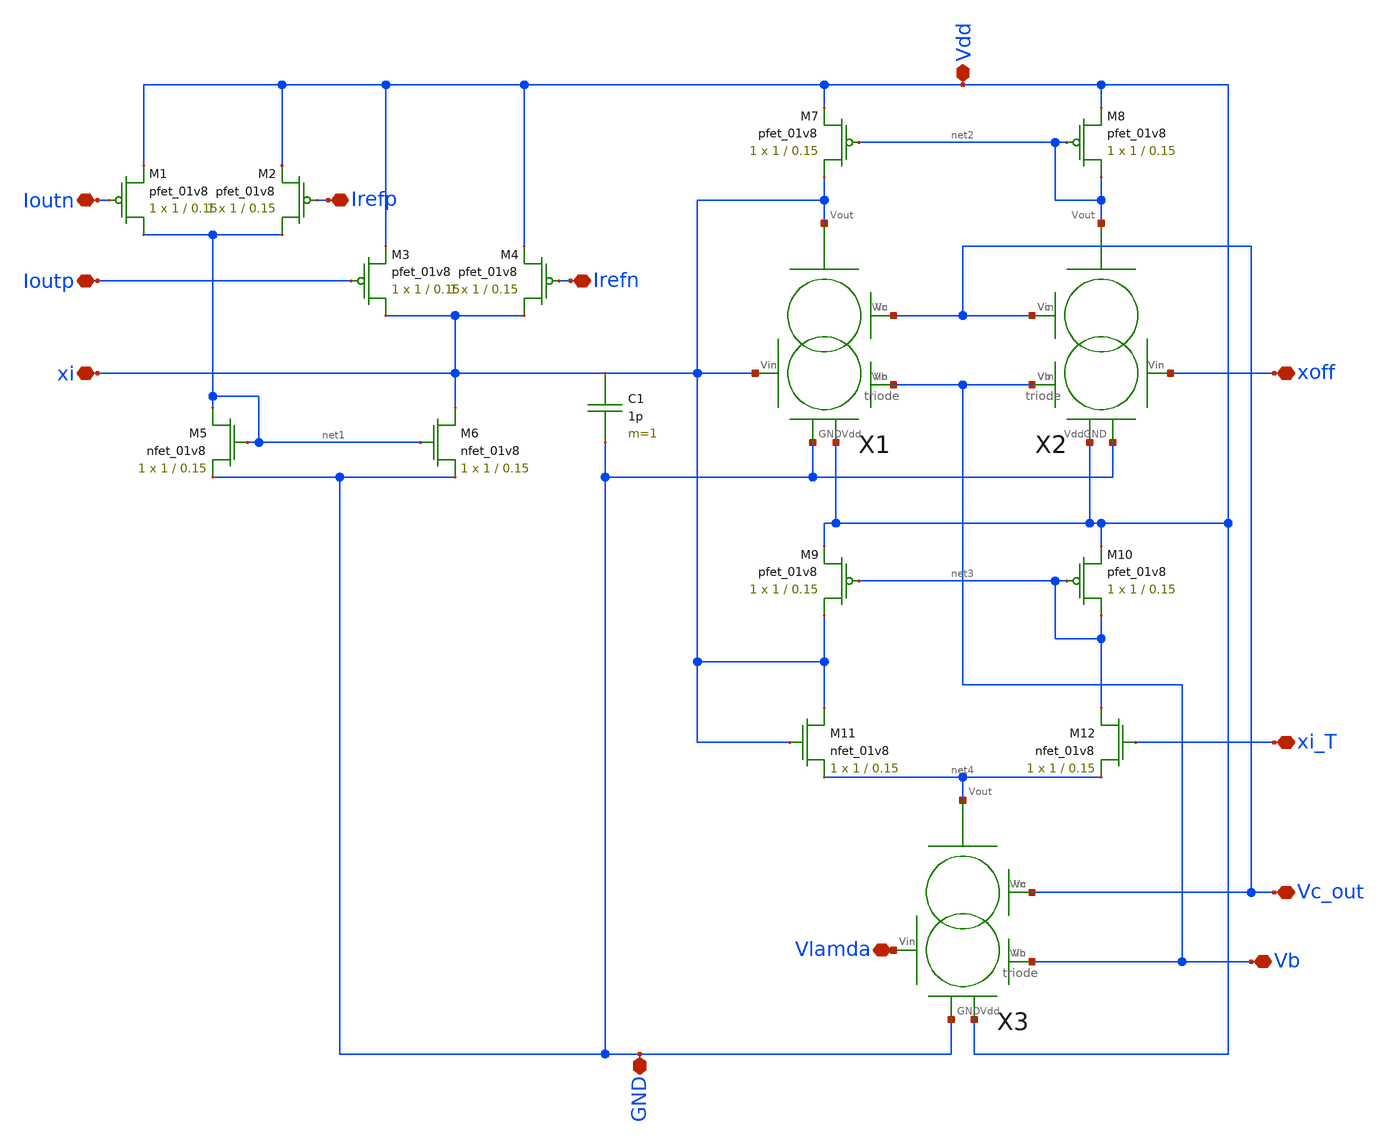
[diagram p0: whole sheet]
** sch_path: neuron.sch
**.subckt neuron Vlamda Vb Vc_out GND Vdd Ioutn Ioutp Irefp Irefn xi xi_T xoff
*.iopin Vlamda
*.iopin Vb
*.iopin Vc_out
*.iopin GND
*.iopin Vdd
*.iopin Ioutn
*.iopin Ioutp
*.iopin Irefp
*.iopin Irefn
*.iopin xi
*.iopin xi_T
*.iopin xoff
XM1 net1 Ioutn Vdd VDD sky130_fd_pr__pfet_01v8 L=0.15 W=1 nf=1 ad='int((nf+1)/2) * W/nf * 0.29' as='int((nf+2)/2) * W/nf * 0.29'
+ pd='2*int((nf+1)/2) * (W/nf + 0.29)' ps='2*int((nf+2)/2) * (W/nf + 0.29)' nrd='0.29 / W' nrs='0.29 / W'
+ sa=0 sb=0 sd=0 mult=1 m=1
XM2 net1 Irefp Vdd VDD sky130_fd_pr__pfet_01v8 L=0.15 W=1 nf=1 ad='int((nf+1)/2) * W/nf * 0.29' as='int((nf+2)/2) * W/nf * 0.29'
+ pd='2*int((nf+1)/2) * (W/nf + 0.29)' ps='2*int((nf+2)/2) * (W/nf + 0.29)' nrd='0.29 / W' nrs='0.29 / W'
+ sa=0 sb=0 sd=0 mult=1 m=1
XM3 Vlamda Ioutp Vdd VDD sky130_fd_pr__pfet_01v8 L=0.15 W=1 nf=1 ad='int((nf+1)/2) * W/nf * 0.29' as='int((nf+2)/2) * W/nf * 0.29'
+ pd='2*int((nf+1)/2) * (W/nf + 0.29)' ps='2*int((nf+2)/2) * (W/nf + 0.29)' nrd='0.29 / W' nrs='0.29 / W'
+ sa=0 sb=0 sd=0 mult=1 m=1
XM4 Vlamda Irefn Vdd VDD sky130_fd_pr__pfet_01v8 L=0.15 W=1 nf=1 ad='int((nf+1)/2) * W/nf * 0.29' as='int((nf+2)/2) * W/nf * 0.29'
+ pd='2*int((nf+1)/2) * (W/nf + 0.29)' ps='2*int((nf+2)/2) * (W/nf + 0.29)' nrd='0.29 / W' nrs='0.29 / W'
+ sa=0 sb=0 sd=0 mult=1 m=1
XM5 net1 net1 GND GND sky130_fd_pr__nfet_01v8 L=0.15 W=1 nf=1 ad='int((nf+1)/2) * W/nf * 0.29' as='int((nf+2)/2) * W/nf * 0.29'
+ pd='2*int((nf+1)/2) * (W/nf + 0.29)' ps='2*int((nf+2)/2) * (W/nf + 0.29)' nrd='0.29 / W' nrs='0.29 / W'
+ sa=0 sb=0 sd=0 mult=1 m=1
XM6 Vlamda net1 GND GND sky130_fd_pr__nfet_01v8 L=0.15 W=1 nf=1 ad='int((nf+1)/2) * W/nf * 0.29' as='int((nf+2)/2) * W/nf * 0.29'
+ pd='2*int((nf+1)/2) * (W/nf + 0.29)' ps='2*int((nf+2)/2) * (W/nf + 0.29)' nrd='0.29 / W' nrs='0.29 / W'
+ sa=0 sb=0 sd=0 mult=1 m=1
C1 Vlamda GND 1p m=1
X1 Vlamda GND Vlamda Vlamda Vlamda Vdd triode
X2 Vlamda GND Vlamda Vlamda net2 Vdd triode
XM7 Vlamda net2 Vdd VDD sky130_fd_pr__pfet_01v8 L=0.15 W=1 nf=1 ad='int((nf+1)/2) * W/nf * 0.29' as='int((nf+2)/2) * W/nf * 0.29'
+ pd='2*int((nf+1)/2) * (W/nf + 0.29)' ps='2*int((nf+2)/2) * (W/nf + 0.29)' nrd='0.29 / W' nrs='0.29 / W'
+ sa=0 sb=0 sd=0 mult=1 m=1
XM8 net2 net2 Vdd VDD sky130_fd_pr__pfet_01v8 L=0.15 W=1 nf=1 ad='int((nf+1)/2) * W/nf * 0.29' as='int((nf+2)/2) * W/nf * 0.29'
+ pd='2*int((nf+1)/2) * (W/nf + 0.29)' ps='2*int((nf+2)/2) * (W/nf + 0.29)' nrd='0.29 / W' nrs='0.29 / W'
+ sa=0 sb=0 sd=0 mult=1 m=1
X3 Vlamda GND Vlamda Vlamda net4 Vdd triode
XM9 Vlamda net3 Vdd VDD sky130_fd_pr__pfet_01v8 L=0.15 W=1 nf=1 ad='int((nf+1)/2) * W/nf * 0.29' as='int((nf+2)/2) * W/nf * 0.29'
+ pd='2*int((nf+1)/2) * (W/nf + 0.29)' ps='2*int((nf+2)/2) * (W/nf + 0.29)' nrd='0.29 / W' nrs='0.29 / W'
+ sa=0 sb=0 sd=0 mult=1 m=1
XM10 net3 net3 Vdd VDD sky130_fd_pr__pfet_01v8 L=0.15 W=1 nf=1 ad='int((nf+1)/2) * W/nf * 0.29' as='int((nf+2)/2) * W/nf * 0.29'
+ pd='2*int((nf+1)/2) * (W/nf + 0.29)' ps='2*int((nf+2)/2) * (W/nf + 0.29)' nrd='0.29 / W' nrs='0.29 / W'
+ sa=0 sb=0 sd=0 mult=1 m=1
XM11 Vlamda Vlamda net4 GND sky130_fd_pr__nfet_01v8 L=0.15 W=1 nf=1 ad='int((nf+1)/2) * W/nf * 0.29'
+ as='int((nf+2)/2) * W/nf * 0.29' pd='2*int((nf+1)/2) * (W/nf + 0.29)' ps='2*int((nf+2)/2) * (W/nf + 0.29)'
+ nrd='0.29 / W' nrs='0.29 / W' sa=0 sb=0 sd=0 mult=1 m=1
XM12 net3 xi_T net4 GND sky130_fd_pr__nfet_01v8 L=0.15 W=1 nf=1 ad='int((nf+1)/2) * W/nf * 0.29' as='int((nf+2)/2) * W/nf * 0.29'
+ pd='2*int((nf+1)/2) * (W/nf + 0.29)' ps='2*int((nf+2)/2) * (W/nf + 0.29)' nrd='0.29 / W' nrs='0.29 / W'
+ sa=0 sb=0 sd=0 mult=1 m=1
**.ends

* expanding   symbol:  /home/ttuser/image_processing_final/triode.sym # of pins=9
** sym_path: triode.sym
** sch_path: triode.sch
.subckt triode Vin GND Vb Vc Vout Vdd
*.iopin Vout
*.iopin Vc
*.iopin Vb
*.iopin Vin
*.iopin GND
*.iopin Vdd
XM7 net4 net1 Vdd VDD sky130_fd_pr__pfet_01v8 L=0.15 W=1 nf=1 ad='int((nf+1)/2) * W/nf * 0.29' as='int((nf+2)/2) * W/nf * 0.29'
+ pd='2*int((nf+1)/2) * (W/nf + 0.29)' ps='2*int((nf+2)/2) * (W/nf + 0.29)' nrd='0.29 / W' nrs='0.29 / W'
+ sa=0 sb=0 sd=0 mult=1 m=1
XM6 net1 net1 Vdd VDD sky130_fd_pr__pfet_01v8 L=0.15 W=1 nf=1 ad='int((nf+1)/2) * W/nf * 0.29' as='int((nf+2)/2) * W/nf * 0.29'
+ pd='2*int((nf+1)/2) * (W/nf + 0.29)' ps='2*int((nf+2)/2) * (W/nf + 0.29)' nrd='0.29 / W' nrs='0.29 / W'
+ sa=0 sb=0 sd=0 mult=1 m=1
XM5 net1 Vc net2 GND sky130_fd_pr__nfet_01v8 L=0.15 W=1 nf=1 ad='int((nf+1)/2) * W/nf * 0.29' as='int((nf+2)/2) * W/nf * 0.29'
+ pd='2*int((nf+1)/2) * (W/nf + 0.29)' ps='2*int((nf+2)/2) * (W/nf + 0.29)' nrd='0.29 / W' nrs='0.29 / W'
+ sa=0 sb=0 sd=0 mult=1 m=1
XM1 GND net3 net2 VDD sky130_fd_pr__pfet_01v8 L=0.15 W=1 nf=1 ad='int((nf+1)/2) * W/nf * 0.29' as='int((nf+2)/2) * W/nf * 0.29'
+ pd='2*int((nf+1)/2) * (W/nf + 0.29)' ps='2*int((nf+2)/2) * (W/nf + 0.29)' nrd='0.29 / W' nrs='0.29 / W'
+ sa=0 sb=0 sd=0 mult=1 m=1
XM2 net4 Vb GND GND sky130_fd_pr__nfet_01v8 L=0.15 W=1 nf=1 ad='int((nf+1)/2) * W/nf * 0.29' as='int((nf+2)/2) * W/nf * 0.29'
+ pd='2*int((nf+1)/2) * (W/nf + 0.29)' ps='2*int((nf+2)/2) * (W/nf + 0.29)' nrd='0.29 / W' nrs='0.29 / W'
+ sa=0 sb=0 sd=0 mult=1 m=1
XM3 net3 Vin GND GND sky130_fd_pr__nfet_01v8 L=0.15 W=1 nf=1 ad='int((nf+1)/2) * W/nf * 0.29' as='int((nf+2)/2) * W/nf * 0.29'
+ pd='2*int((nf+1)/2) * (W/nf + 0.29)' ps='2*int((nf+2)/2) * (W/nf + 0.29)' nrd='0.29 / W' nrs='0.29 / W'
+ sa=0 sb=0 sd=0 mult=1 m=1
XM4 Vout net4 net3 GND sky130_fd_pr__nfet_01v8 L=0.15 W=1 nf=1 ad='int((nf+1)/2) * W/nf * 0.29' as='int((nf+2)/2) * W/nf * 0.29'
+ pd='2*int((nf+1)/2) * (W/nf + 0.29)' ps='2*int((nf+2)/2) * (W/nf + 0.29)' nrd='0.29 / W' nrs='0.29 / W'
+ sa=0 sb=0 sd=0 mult=1 m=1
.ends

.end
